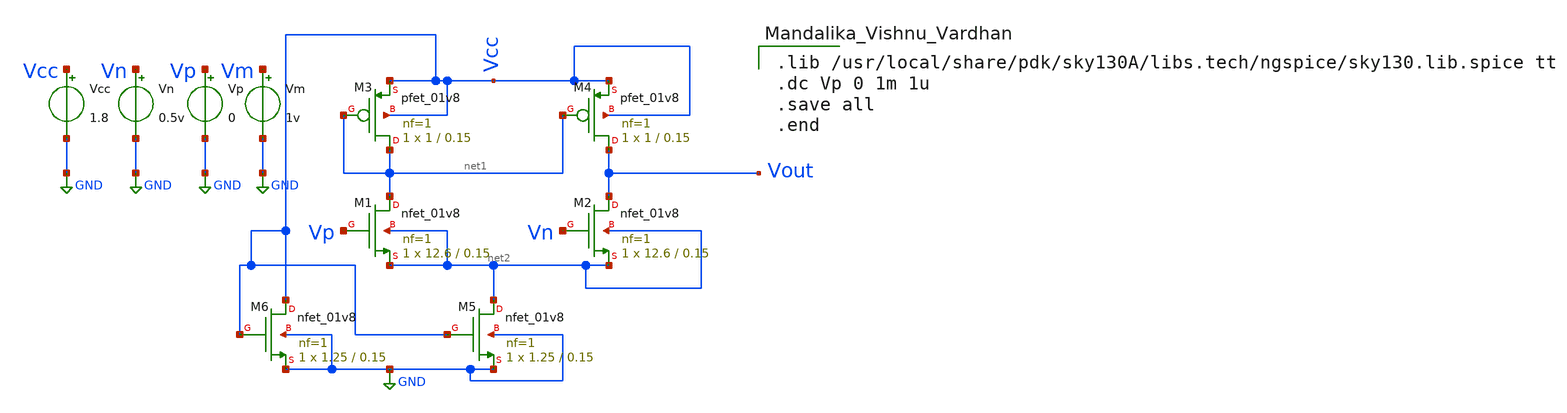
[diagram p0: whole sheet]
** sch_path: SSOpAmp.sch
**.subckt SSOpAmp
XM1 net1 Vp net2 net2 sky130_fd_pr__nfet_01v8 L=0.15 W=12.6 nf=1 ad='int((nf+1)/2) * W/nf * 0.29' as='int((nf+2)/2) * W/nf * 0.29'
+ pd='2*int((nf+1)/2) * (W/nf + 0.29)' ps='2*int((nf+2)/2) * (W/nf + 0.29)' nrd='0.29 / W' nrs='0.29 / W'
+ sa=0 sb=0 sd=0 mult=1 m=1
XM2 Vout Vn net2 net2 sky130_fd_pr__nfet_01v8 L=0.15 W=12.6 nf=1 ad='int((nf+1)/2) * W/nf * 0.29' as='int((nf+2)/2) * W/nf * 0.29'
+ pd='2*int((nf+1)/2) * (W/nf + 0.29)' ps='2*int((nf+2)/2) * (W/nf + 0.29)' nrd='0.29 / W' nrs='0.29 / W'
+ sa=0 sb=0 sd=0 mult=1 m=1
XM3 net1 net1 Vcc Vcc sky130_fd_pr__pfet_01v8 L=0.15 W=1 nf=1 ad='int((nf+1)/2) * W/nf * 0.29' as='int((nf+2)/2) * W/nf * 0.29'
+ pd='2*int((nf+1)/2) * (W/nf + 0.29)' ps='2*int((nf+2)/2) * (W/nf + 0.29)' nrd='0.29 / W' nrs='0.29 / W'
+ sa=0 sb=0 sd=0 mult=1 m=1
XM4 Vout net1 Vcc Vcc sky130_fd_pr__pfet_01v8 L=0.15 W=1 nf=1 ad='int((nf+1)/2) * W/nf * 0.29' as='int((nf+2)/2) * W/nf * 0.29'
+ pd='2*int((nf+1)/2) * (W/nf + 0.29)' ps='2*int((nf+2)/2) * (W/nf + 0.29)' nrd='0.29 / W' nrs='0.29 / W'
+ sa=0 sb=0 sd=0 mult=1 m=1
XM5 net2 Vcc GND GND sky130_fd_pr__nfet_01v8 L=0.15 W=1.25 nf=1 ad='int((nf+1)/2) * W/nf * 0.29' as='int((nf+2)/2) * W/nf * 0.29'
+ pd='2*int((nf+1)/2) * (W/nf + 0.29)' ps='2*int((nf+2)/2) * (W/nf + 0.29)' nrd='0.29 / W' nrs='0.29 / W'
+ sa=0 sb=0 sd=0 mult=1 m=1
Vcc Vcc GND 1.8
Vn Vn GND 0.5v
Vp Vp GND 0
Vm Vm GND 1v
XM6 Vcc Vcc GND GND sky130_fd_pr__nfet_01v8 L=0.15 W=1.25 nf=1 ad='int((nf+1)/2) * W/nf * 0.29' as='int((nf+2)/2) * W/nf * 0.29'
+ pd='2*int((nf+1)/2) * (W/nf + 0.29)' ps='2*int((nf+2)/2) * (W/nf + 0.29)' nrd='0.29 / W' nrs='0.29 / W'
+ sa=0 sb=0 sd=0 mult=1 m=1
**** begin user architecture code

.lib /usr/local/share/pdk/sky130A/libs.tech/ngspice/sky130.lib.spice tt
.dc Vp 0 1m 1u
.save all
.end

**** end user architecture code
**.ends
.GLOBAL GND
.end
